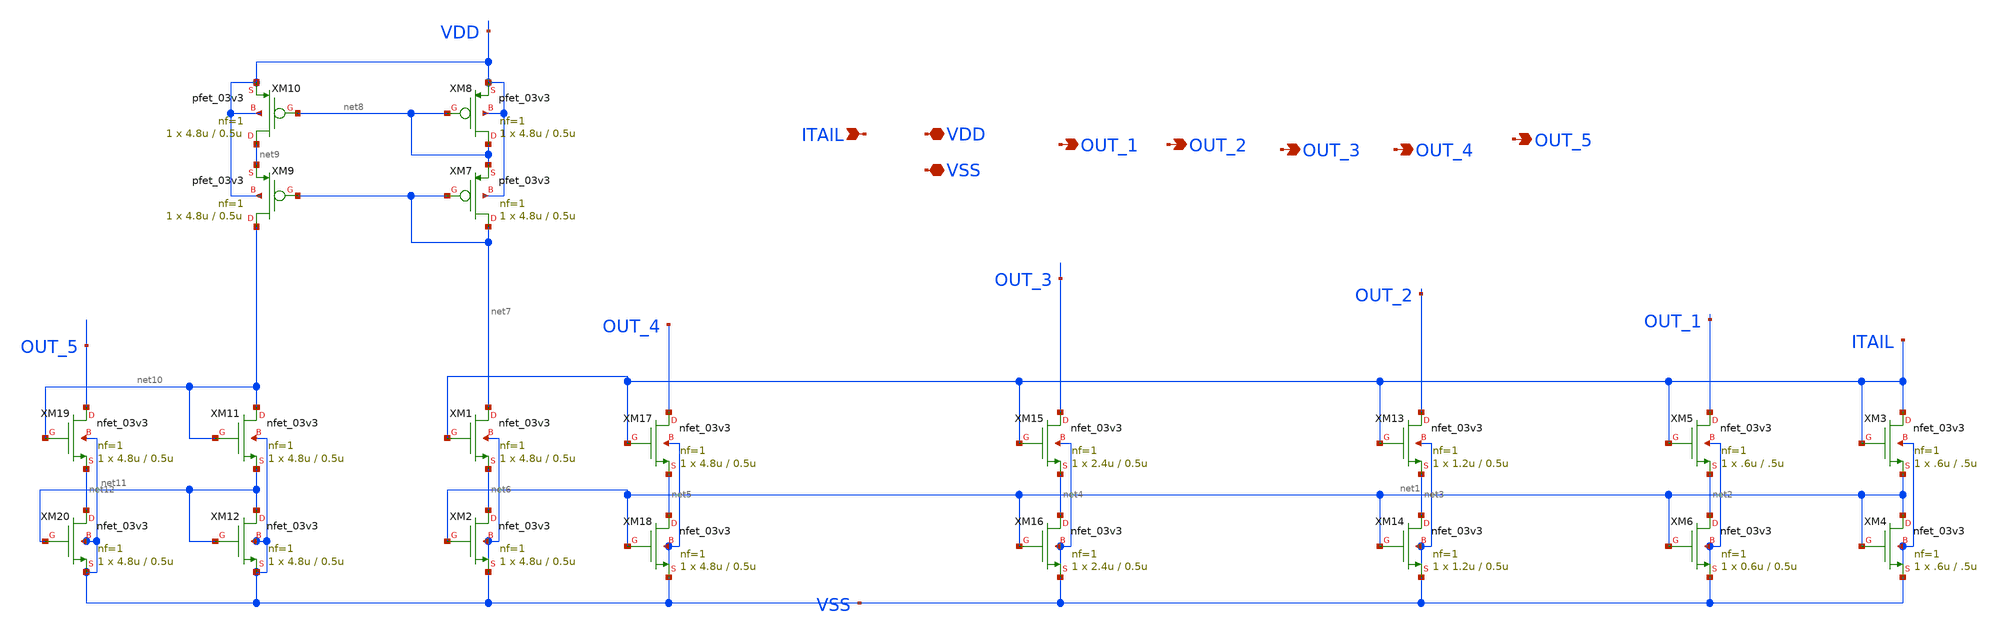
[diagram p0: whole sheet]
** sch_path: DAC_PAKISTAN_01/Pakistan1_Xschem/untitled-21.sch
**.subckt untitled-21 ITAIL VDD VSS OUT_1 OUT_2 OUT_3 OUT_4 OUT_5
*.ipin ITAIL
*.iopin VDD
*.iopin VSS
*.opin OUT_1
*.opin OUT_2
*.opin OUT_3
*.opin OUT_4
*.opin OUT_5
XM3 ITAIL ITAIL net1 VSS nfet_03v3 L=.5u W=.6u nf=1 ad='int((nf+1)/2) * W/nf * 0.18u' as='int((nf+2)/2) * W/nf * 0.18u'
+ pd='2*int((nf+1)/2) * (W/nf + 0.18u)' ps='2*int((nf+2)/2) * (W/nf + 0.18u)' nrd='0.18u / W' nrs='0.18u / W'
+ sa=0 sb=0 sd=0 m=1
XM4 net1 net1 VSS VSS nfet_03v3 L=.5u W=.6u nf=1 ad='int((nf+1)/2) * W/nf * 0.18u' as='int((nf+2)/2) * W/nf * 0.18u'
+ pd='2*int((nf+1)/2) * (W/nf + 0.18u)' ps='2*int((nf+2)/2) * (W/nf + 0.18u)' nrd='0.18u / W' nrs='0.18u / W'
+ sa=0 sb=0 sd=0 m=1
XM5 OUT_1 ITAIL net2 VSS nfet_03v3 L=.5u W=.6u nf=1 ad='int((nf+1)/2) * W/nf * 0.18u' as='int((nf+2)/2) * W/nf * 0.18u'
+ pd='2*int((nf+1)/2) * (W/nf + 0.18u)' ps='2*int((nf+2)/2) * (W/nf + 0.18u)' nrd='0.18u / W' nrs='0.18u / W'
+ sa=0 sb=0 sd=0 m=1
XM6 net2 net1 VSS VSS nfet_03v3 L=0.5u W=0.6u nf=1 ad='int((nf+1)/2) * W/nf * 0.18u' as='int((nf+2)/2) * W/nf * 0.18u'
+ pd='2*int((nf+1)/2) * (W/nf + 0.18u)' ps='2*int((nf+2)/2) * (W/nf + 0.18u)' nrd='0.18u / W' nrs='0.18u / W'
+ sa=0 sb=0 sd=0 m=1
XM13 OUT_2 ITAIL net3 VSS nfet_03v3 L=0.5u W=1.2u nf=1 ad='int((nf+1)/2) * W/nf * 0.18u' as='int((nf+2)/2) * W/nf * 0.18u'
+ pd='2*int((nf+1)/2) * (W/nf + 0.18u)' ps='2*int((nf+2)/2) * (W/nf + 0.18u)' nrd='0.18u / W' nrs='0.18u / W'
+ sa=0 sb=0 sd=0 m=1
XM14 net3 net1 VSS VSS nfet_03v3 L=0.5u W=1.2u nf=1 ad='int((nf+1)/2) * W/nf * 0.18u' as='int((nf+2)/2) * W/nf * 0.18u'
+ pd='2*int((nf+1)/2) * (W/nf + 0.18u)' ps='2*int((nf+2)/2) * (W/nf + 0.18u)' nrd='0.18u / W' nrs='0.18u / W'
+ sa=0 sb=0 sd=0 m=1
XM15 OUT_3 ITAIL net4 VSS nfet_03v3 L=0.5u W=2.4u nf=1 ad='int((nf+1)/2) * W/nf * 0.18u' as='int((nf+2)/2) * W/nf * 0.18u'
+ pd='2*int((nf+1)/2) * (W/nf + 0.18u)' ps='2*int((nf+2)/2) * (W/nf + 0.18u)' nrd='0.18u / W' nrs='0.18u / W'
+ sa=0 sb=0 sd=0 m=1
XM16 net4 net1 VSS VSS nfet_03v3 L=0.5u W=2.4u nf=1 ad='int((nf+1)/2) * W/nf * 0.18u' as='int((nf+2)/2) * W/nf * 0.18u'
+ pd='2*int((nf+1)/2) * (W/nf + 0.18u)' ps='2*int((nf+2)/2) * (W/nf + 0.18u)' nrd='0.18u / W' nrs='0.18u / W'
+ sa=0 sb=0 sd=0 m=1
XM17 OUT_4 ITAIL net5 VSS nfet_03v3 L=0.5u W=4.8u nf=1 ad='int((nf+1)/2) * W/nf * 0.18u' as='int((nf+2)/2) * W/nf * 0.18u'
+ pd='2*int((nf+1)/2) * (W/nf + 0.18u)' ps='2*int((nf+2)/2) * (W/nf + 0.18u)' nrd='0.18u / W' nrs='0.18u / W'
+ sa=0 sb=0 sd=0 m=1
XM18 net5 net1 VSS VSS nfet_03v3 L=0.5u W=4.8u nf=1 ad='int((nf+1)/2) * W/nf * 0.18u' as='int((nf+2)/2) * W/nf * 0.18u'
+ pd='2*int((nf+1)/2) * (W/nf + 0.18u)' ps='2*int((nf+2)/2) * (W/nf + 0.18u)' nrd='0.18u / W' nrs='0.18u / W'
+ sa=0 sb=0 sd=0 m=1
XM1 net7 ITAIL net6 VSS nfet_03v3 L=0.5u W=4.8u nf=1 ad='int((nf+1)/2) * W/nf * 0.18u' as='int((nf+2)/2) * W/nf * 0.18u'
+ pd='2*int((nf+1)/2) * (W/nf + 0.18u)' ps='2*int((nf+2)/2) * (W/nf + 0.18u)' nrd='0.18u / W' nrs='0.18u / W'
+ sa=0 sb=0 sd=0 m=1
XM2 net6 net1 VSS VSS nfet_03v3 L=0.5u W=4.8u nf=1 ad='int((nf+1)/2) * W/nf * 0.18u' as='int((nf+2)/2) * W/nf * 0.18u'
+ pd='2*int((nf+1)/2) * (W/nf + 0.18u)' ps='2*int((nf+2)/2) * (W/nf + 0.18u)' nrd='0.18u / W' nrs='0.18u / W'
+ sa=0 sb=0 sd=0 m=1
XM7 net7 net7 net8 VDD pfet_03v3 L=0.5u W=4.8u nf=1 ad='int((nf+1)/2) * W/nf * 0.18u' as='int((nf+2)/2) * W/nf * 0.18u'
+ pd='2*int((nf+1)/2) * (W/nf + 0.18u)' ps='2*int((nf+2)/2) * (W/nf + 0.18u)' nrd='0.18u / W' nrs='0.18u / W'
+ sa=0 sb=0 sd=0 m=1
XM8 net8 net8 VDD VDD pfet_03v3 L=0.5u W=4.8u nf=1 ad='int((nf+1)/2) * W/nf * 0.18u' as='int((nf+2)/2) * W/nf * 0.18u'
+ pd='2*int((nf+1)/2) * (W/nf + 0.18u)' ps='2*int((nf+2)/2) * (W/nf + 0.18u)' nrd='0.18u / W' nrs='0.18u / W'
+ sa=0 sb=0 sd=0 m=1
XM9 net10 net7 net9 VDD pfet_03v3 L=0.5u W=4.8u nf=1 ad='int((nf+1)/2) * W/nf * 0.18u' as='int((nf+2)/2) * W/nf * 0.18u'
+ pd='2*int((nf+1)/2) * (W/nf + 0.18u)' ps='2*int((nf+2)/2) * (W/nf + 0.18u)' nrd='0.18u / W' nrs='0.18u / W'
+ sa=0 sb=0 sd=0 m=1
XM10 net9 net8 VDD VDD pfet_03v3 L=0.5u W=4.8u nf=1 ad='int((nf+1)/2) * W/nf * 0.18u' as='int((nf+2)/2) * W/nf * 0.18u'
+ pd='2*int((nf+1)/2) * (W/nf + 0.18u)' ps='2*int((nf+2)/2) * (W/nf + 0.18u)' nrd='0.18u / W' nrs='0.18u / W'
+ sa=0 sb=0 sd=0 m=1
XM11 net10 net10 net11 VSS nfet_03v3 L=0.5u W=4.8u nf=1 ad='int((nf+1)/2) * W/nf * 0.18u' as='int((nf+2)/2) * W/nf * 0.18u'
+ pd='2*int((nf+1)/2) * (W/nf + 0.18u)' ps='2*int((nf+2)/2) * (W/nf + 0.18u)' nrd='0.18u / W' nrs='0.18u / W'
+ sa=0 sb=0 sd=0 m=1
XM12 net11 net11 VSS VSS nfet_03v3 L=0.5u W=4.8u nf=1 ad='int((nf+1)/2) * W/nf * 0.18u' as='int((nf+2)/2) * W/nf * 0.18u'
+ pd='2*int((nf+1)/2) * (W/nf + 0.18u)' ps='2*int((nf+2)/2) * (W/nf + 0.18u)' nrd='0.18u / W' nrs='0.18u / W'
+ sa=0 sb=0 sd=0 m=1
XM19 OUT_5 net10 net12 VSS nfet_03v3 L=0.5u W=4.8u nf=1 ad='int((nf+1)/2) * W/nf * 0.18u' as='int((nf+2)/2) * W/nf * 0.18u'
+ pd='2*int((nf+1)/2) * (W/nf + 0.18u)' ps='2*int((nf+2)/2) * (W/nf + 0.18u)' nrd='0.18u / W' nrs='0.18u / W'
+ sa=0 sb=0 sd=0 m=1
XM20 net12 net11 VSS VSS nfet_03v3 L=0.5u W=4.8u nf=1 ad='int((nf+1)/2) * W/nf * 0.18u' as='int((nf+2)/2) * W/nf * 0.18u'
+ pd='2*int((nf+1)/2) * (W/nf + 0.18u)' ps='2*int((nf+2)/2) * (W/nf + 0.18u)' nrd='0.18u / W' nrs='0.18u / W'
+ sa=0 sb=0 sd=0 m=1
**.ends
.end
